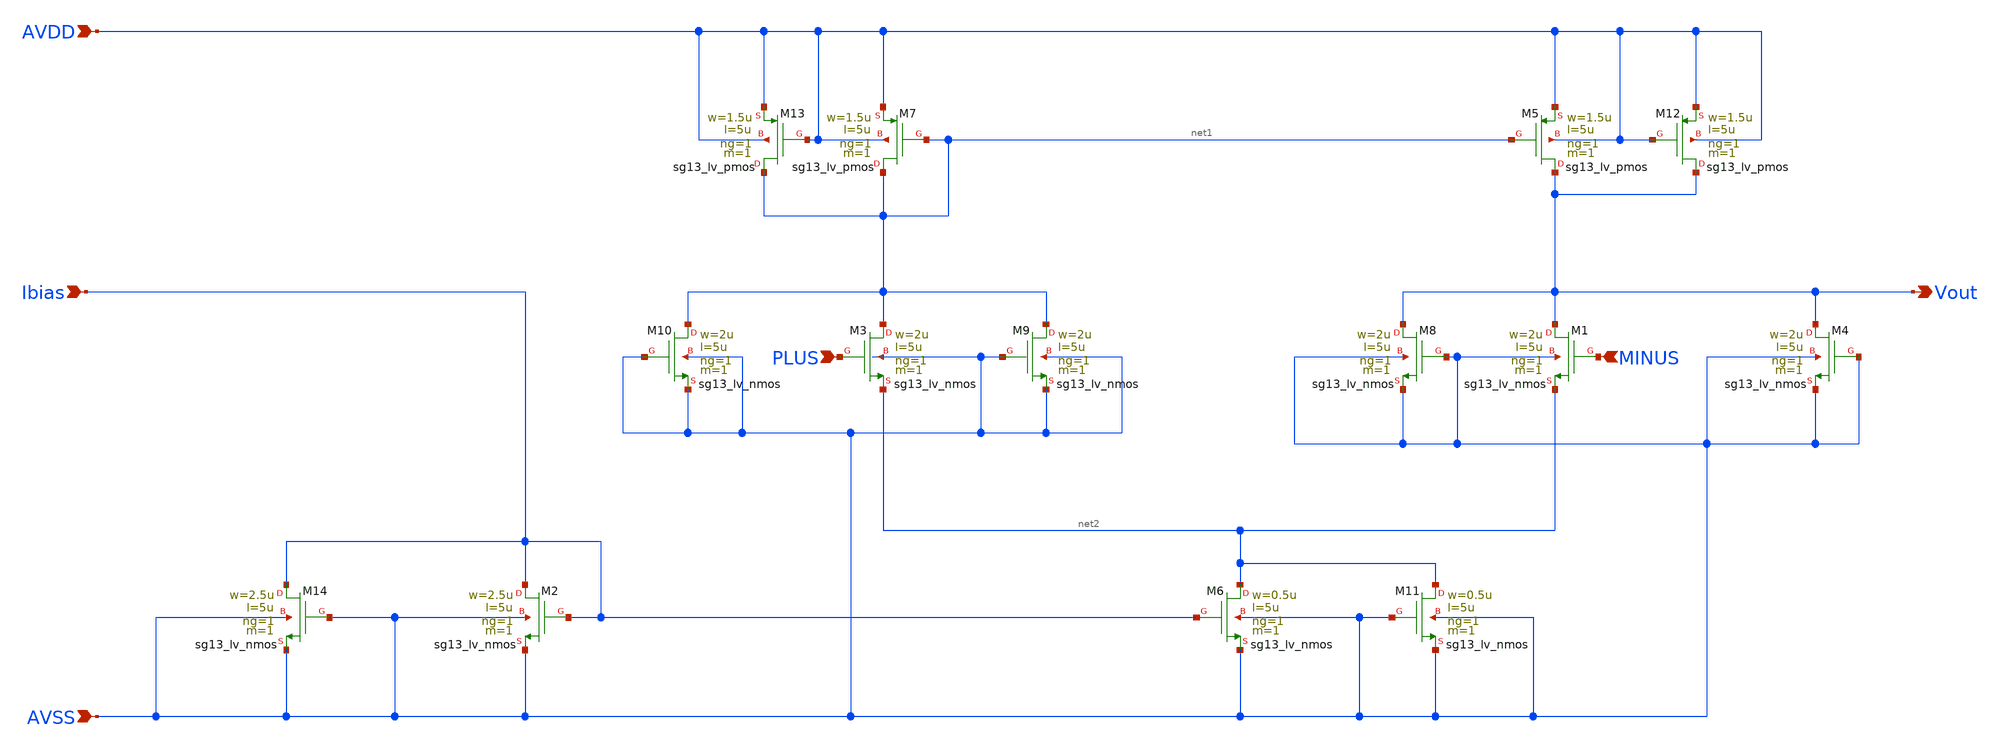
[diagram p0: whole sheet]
** sch_path: Designs/otas/1_schematics/5tota.sch
* (c) 2025 Thesis_HP, Apache-2.0 license
**.subckt 5tota PLUS AVDD Ibias AVSS MINUS Vout
*.ipin PLUS
*.ipin AVDD
*.ipin Ibias
*.ipin AVSS
*.ipin MINUS
*.opin Vout
XM3 net1 PLUS net2 AVSS sg13_lv_nmos w=2u l=5u ng=1 m=1 mm_ok=1
XM5 Vout net1 AVDD AVDD sg13_lv_pmos w=1.5u l=5u ng=1 m=1 mm_ok=1
XM7 net1 net1 AVDD AVDD sg13_lv_pmos w=1.5u l=5u ng=1 m=1 mm_ok=1
XM9 net1 AVSS AVSS AVSS sg13_lv_nmos w=2u l=5u ng=1 m=1 mm_ok=1
XM10 net1 AVSS AVSS AVSS sg13_lv_nmos w=2u l=5u ng=1 m=1 mm_ok=1
XM12 Vout AVDD AVDD AVDD sg13_lv_pmos w=1.5u l=5u ng=1 m=1 mm_ok=1
XM13 net1 AVDD AVDD AVDD sg13_lv_pmos w=1.5u l=5u ng=1 m=1 mm_ok=1
XM6 net2 Ibias AVSS AVSS sg13_lv_nmos w=0.5u l=5u ng=1 m=1 mm_ok=1
XM2 Ibias Ibias AVSS AVSS sg13_lv_nmos w=2.5u l=5u ng=1 m=1 mm_ok=1
XM11 net2 AVSS AVSS AVSS sg13_lv_nmos w=0.5u l=5u ng=1 m=1 mm_ok=1
XM1 Vout MINUS net2 AVSS sg13_lv_nmos w=2u l=5u ng=1 m=1 mm_ok=1
XM4 Vout AVSS AVSS AVSS sg13_lv_nmos w=2u l=5u ng=1 m=1 mm_ok=1
XM8 Vout AVSS AVSS AVSS sg13_lv_nmos w=2u l=5u ng=1 m=1 mm_ok=1
XM14 Ibias AVSS AVSS AVSS sg13_lv_nmos w=2.5u l=5u ng=1 m=1 mm_ok=1
**.ends
.end
